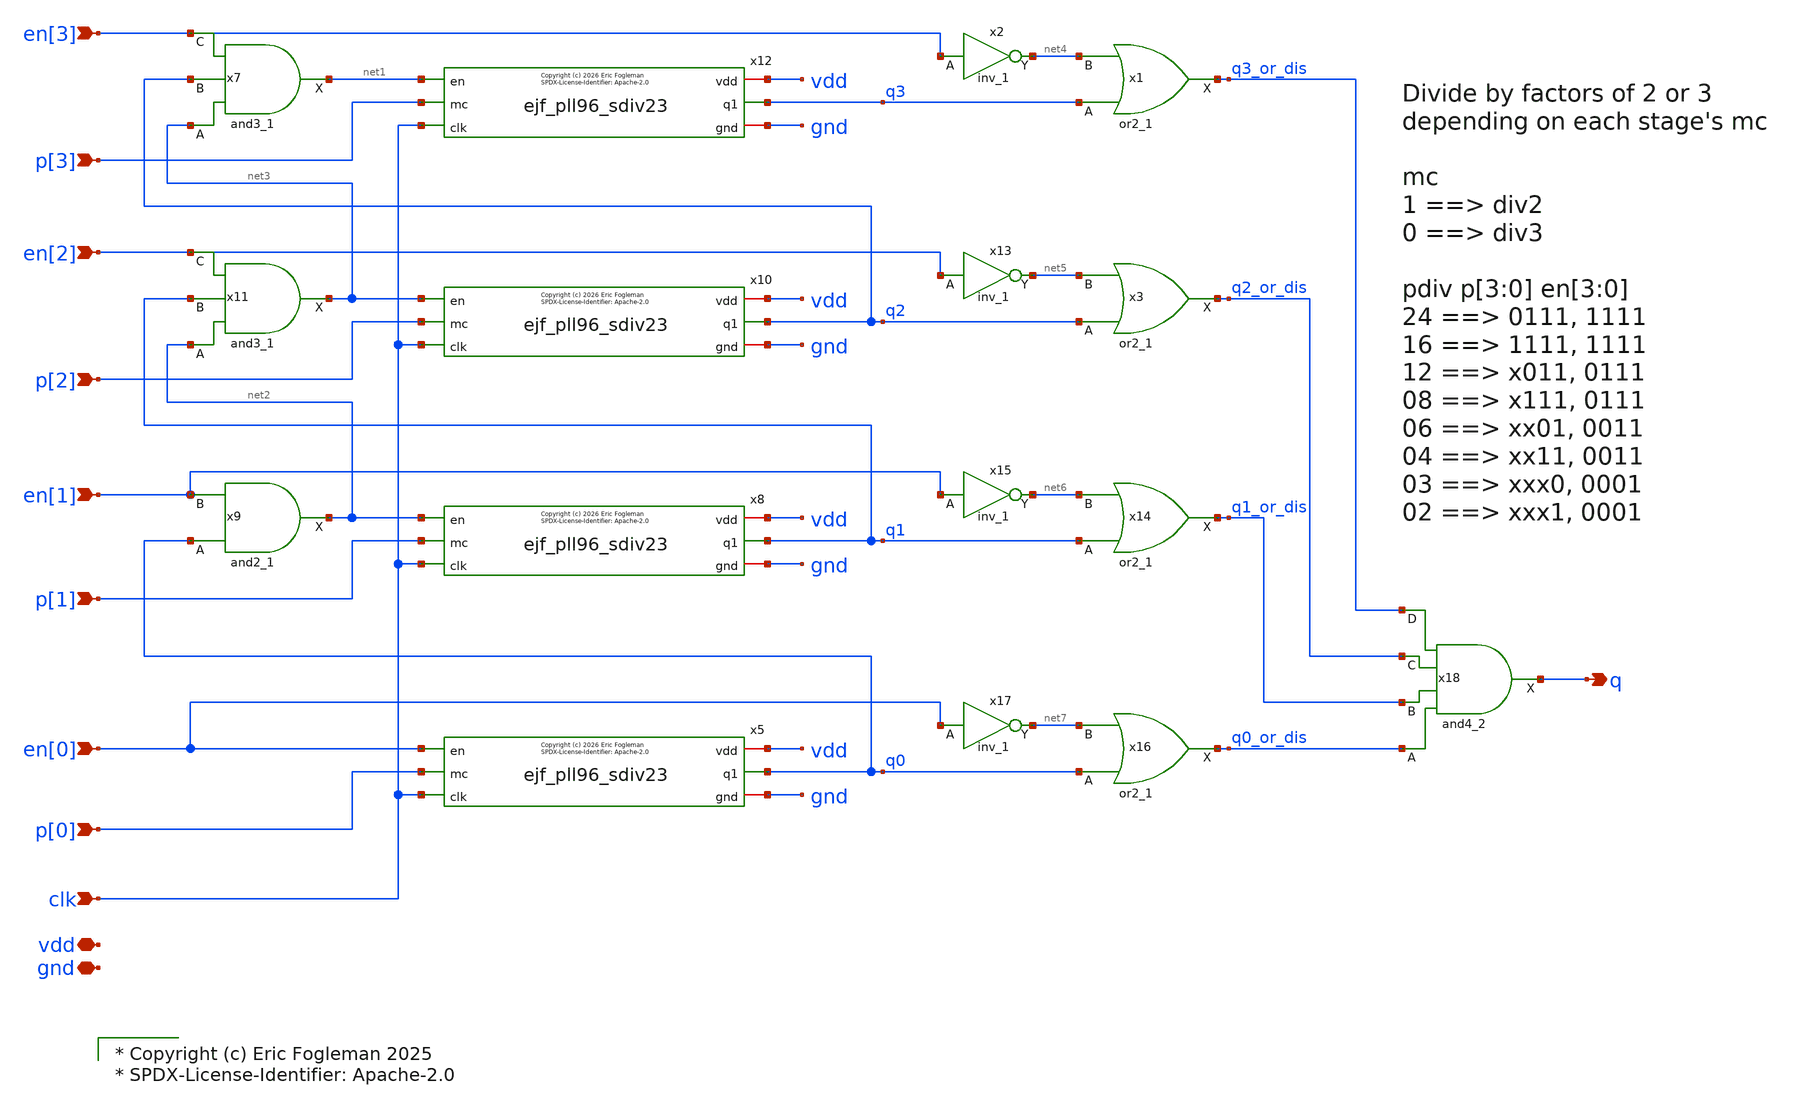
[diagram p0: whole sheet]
** sch_path: xschem/ejf_pll96_sdiv_p.sch
* xschem/ejf_pll96_sdiv23.sym:
* Copyright (c) 2026 Eric Fogleman

* Copyright (c) Eric Fogleman 2025
* SPDX-License-Identifier: Apache-2.0

**.subckt ejf_pll96_sdiv_p vdd gnd clk p[1] p[2] p[3] en[3] en[2] q en[1] p[0] en[0]
*.iopin vdd
*.iopin gnd
*.ipin clk
*.ipin p[1]
*.ipin p[2]
*.ipin p[3]
*.ipin en[3]
*.ipin en[2]
*.opin q
*.ipin en[1]
*.ipin p[0]
*.ipin en[0]
x5 q0 clk p[0] vdd gnd en[0] ejf_pll96_sdiv23
x8 q1 clk p[1] vdd gnd net2 ejf_pll96_sdiv23
x9 q0 en[1] gnd gnd vdd vdd net2 sky130_fd_sc_ls__and2_1
x10 q2 clk p[2] vdd gnd net3 ejf_pll96_sdiv23
x11 net2 q1 en[2] gnd gnd vdd vdd net3 sky130_fd_sc_ls__and3_1
x12 q3 clk p[3] vdd gnd net1 ejf_pll96_sdiv23
x7 net3 q2 en[3] gnd gnd vdd vdd net1 sky130_fd_sc_ls__and3_1
x1 q3 net4 gnd gnd vdd vdd q3_or_dis sky130_fd_sc_ls__or2_1
x2 en[3] gnd gnd vdd vdd net4 sky130_fd_sc_ls__inv_1
x3 q2 net5 gnd gnd vdd vdd q2_or_dis sky130_fd_sc_ls__or2_1
x13 en[2] gnd gnd vdd vdd net5 sky130_fd_sc_ls__inv_1
x14 q1 net6 gnd gnd vdd vdd q1_or_dis sky130_fd_sc_ls__or2_1
x15 en[1] gnd gnd vdd vdd net6 sky130_fd_sc_ls__inv_1
x16 q0 net7 gnd gnd vdd vdd q0_or_dis sky130_fd_sc_ls__or2_1
x17 en[0] gnd gnd vdd vdd net7 sky130_fd_sc_ls__inv_1
x18 q0_or_dis q1_or_dis q2_or_dis q3_or_dis gnd gnd vdd vdd q sky130_fd_sc_ls__and4_2
**.ends

* expanding   symbol:  ejf_pll96_sdiv23.sym # of pins=6
** sym_path: xschem/ejf_pll96_sdiv23.sym
** sch_path: xschem/ejf_pll96_sdiv23.sch
.subckt ejf_pll96_sdiv23 q1 clk mc vdd gnd en
*.ipin clk
*.ipin mc
*.opin q1
*.iopin vdd
*.iopin gnd
*.ipin en
x3 q1 mc net1 gnd gnd vdd vdd d2 sky130_fd_sc_ls__o21a_1
**** begin user architecture code

* Copyright (c) Eric Fogleman 2026
* SPDX-License-Identifier: Apache-2.0

**** end user architecture code
x1 clk net1 en gnd gnd vdd vdd q1 sky130_fd_sc_ls__edfxtp_1
x2 clk d2 en gnd gnd vdd vdd q2 net1 sky130_fd_sc_ls__edfxbp_1
.ends

.end
